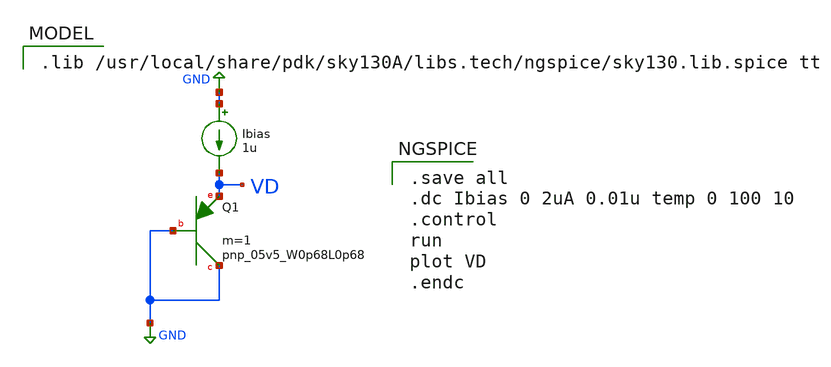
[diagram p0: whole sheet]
** sch_path: 1_diode_0p68_Ibias_varying.sch
**.subckt 1_diode_0p68_Ibias_varying
XQ1 GND GND VD sky130_fd_pr__pnp_05v5_W0p68L0p68 m=1
Ibias GND VD 1u
**** begin user architecture code

.save all
.dc Ibias 0 2uA 0.01u temp 0 100 10
.control
run
plot VD
.endc


.lib /usr/local/share/pdk/sky130A/libs.tech/ngspice/sky130.lib.spice tt

**** end user architecture code
**.ends
.GLOBAL GND
.end
